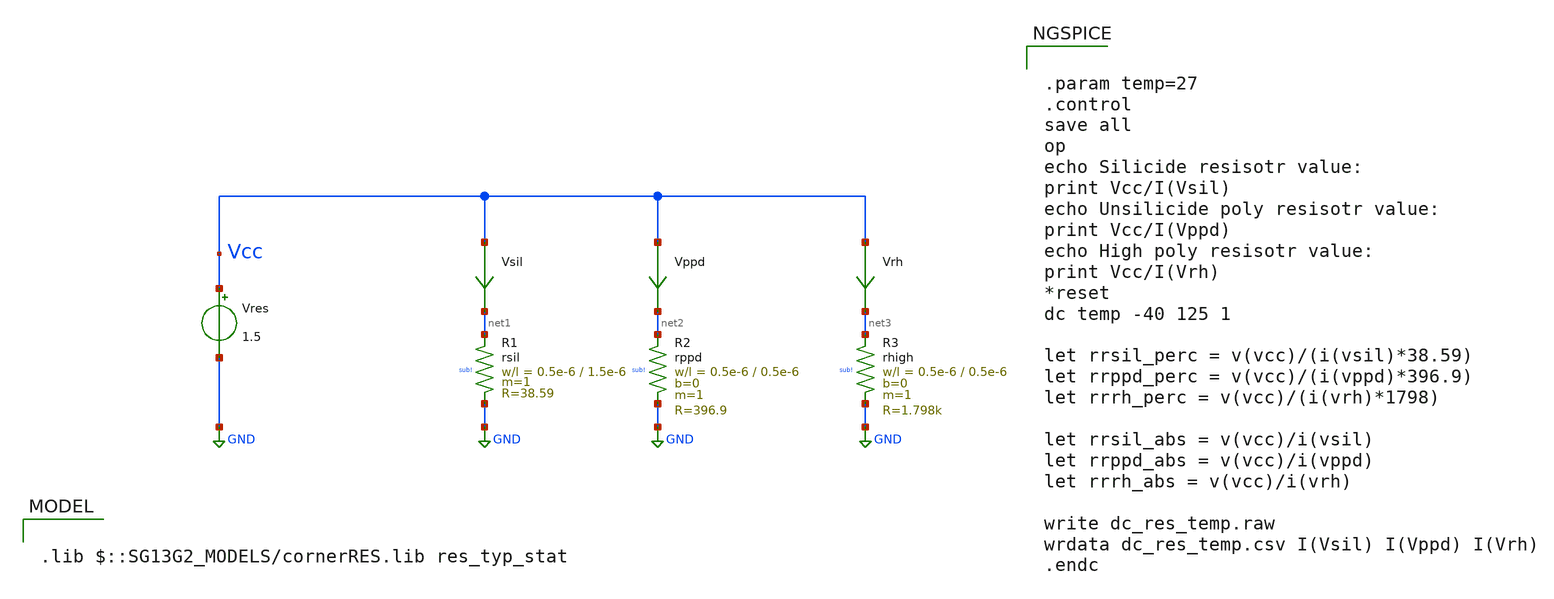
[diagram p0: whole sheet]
** sch_path: TempSensor/design_data/xschem/device_testbenches/dc_res_temp.sch
* Copyright 2023 IHP PDK Authors
**.subckt dc_res_temp
Vres Vcc GND 1.5
Vsil Vcc net1 0
.save i(vsil)
Vppd Vcc net2 0
.save i(vppd)
Vrh Vcc net3 0
.save i(vrh)
XR1 net1 GND sub! rsil w=0.5e-6 l=1.5e-6 m=1 mm_ok=1
XR2 net2 GND sub! rppd w=0.5e-6 l=0.5e-6 m=1 b=0 mm_ok=1
XR3 net3 GND sub! rhigh w=0.5e-6 l=0.5e-6 m=1 b=0 mm_ok=1
**** begin user architecture code

.lib $::SG13G2_MODELS/cornerRES.lib res_typ_stat



.param temp=27
.control
save all
op
echo Silicide resisotr value:
print Vcc/I(Vsil)
echo Unsilicide poly resisotr value:
print Vcc/I(Vppd)
echo High poly resisotr value:
print Vcc/I(Vrh)
*reset
dc temp -40 125 1

let rrsil_perc = v(vcc)/(i(vsil)*38.59)
let rrppd_perc = v(vcc)/(i(vppd)*396.9)
let rrrh_perc = v(vcc)/(i(vrh)*1798)

let rrsil_abs = v(vcc)/i(vsil)
let rrppd_abs = v(vcc)/i(vppd)
let rrrh_abs = v(vcc)/i(vrh)

write dc_res_temp.raw
wrdata dc_res_temp.csv I(Vsil) I(Vppd) I(Vrh)
.endc


**** end user architecture code
**.ends
.GLOBAL GND
.end
